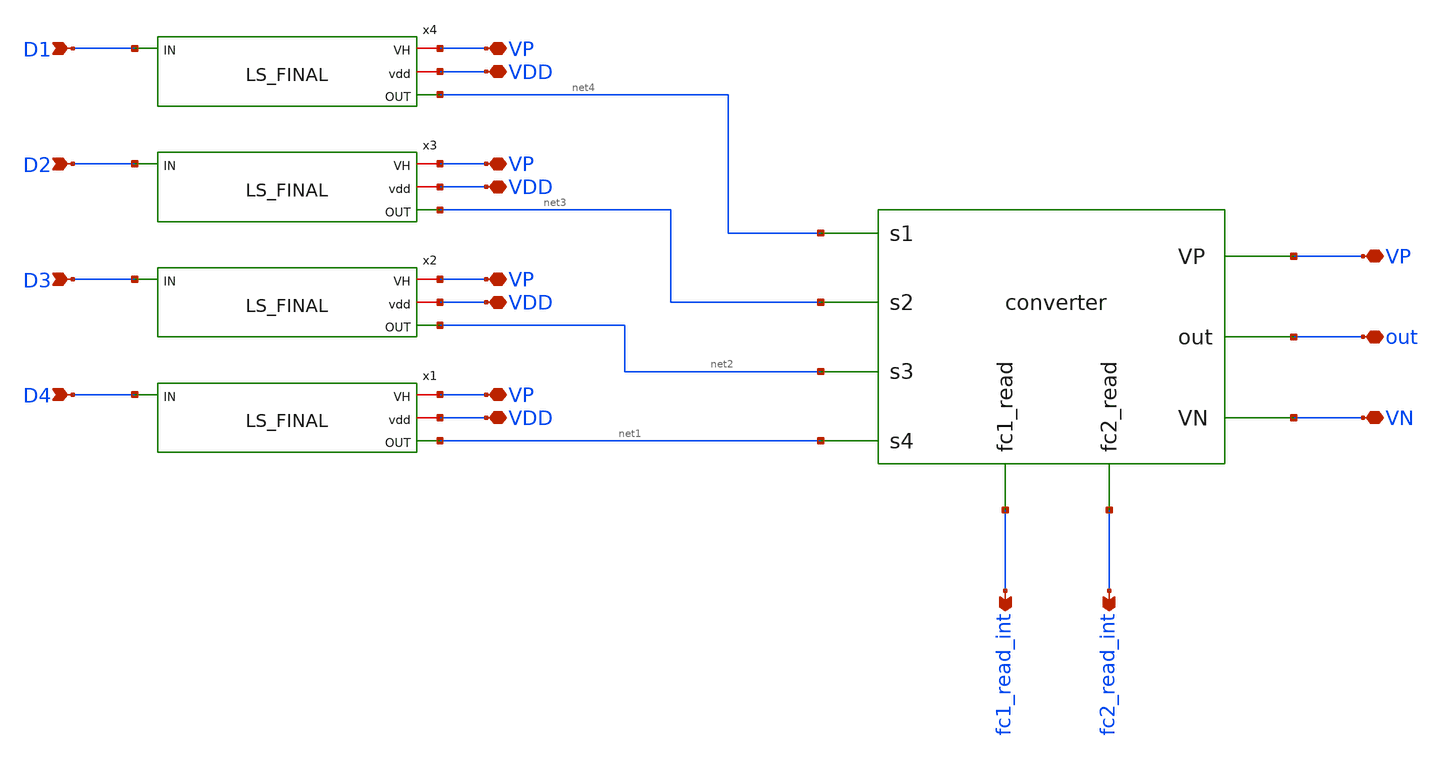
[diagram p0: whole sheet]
** sch_path: xschem/hierarchy_sch/interleaved.sch
**.subckt interleaved VN D1 D2 D3 D4 fc1_read_int fc2_read_int VP VP VP VP VP VDD VDD VDD VDD out
*.iopin VN
*.ipin D1
*.ipin D2
*.ipin D3
*.ipin D4
*.opin fc1_read_int
*.opin fc2_read_int
*.iopin VP
*.iopin VP
*.iopin VP
*.iopin VP
*.iopin VP
*.iopin VDD
*.iopin VDD
*.iopin VDD
*.iopin VDD
*.iopin out
x1 VP VDD net1 D4 LS_FINAL
x2 VP VDD net2 D3 LS_FINAL
x3 VP VDD net3 D2 LS_FINAL
x4 VP VDD net4 D1 LS_FINAL
X1 net4 net3 net2 net1 out VP VN fc1_read_int fc2_read_int converter
**.ends

* expanding   symbol:  personal/3LFCC_AC3E/xschem/dev_switches/DCDC_5V_FINAL/LS_FINAL.sym # of
*+ pins=4
** sym_path: xschem/dev_switches/DCDC_5V_FINAL/LS_FINAL.sym
** sch_path: xschem/dev_switches/DCDC_5V_FINAL/LS_FINAL.sch
.subckt LS_FINAL VH vdd OUT IN
*.ipin IN
*.iopin vdd
*.iopin VH
*.opin OUT
XM11 net1 IN vdd vdd sky130_fd_pr__pfet_01v8 L=0.15 W=5 nf=1 ad='int((nf+1)/2) * W/nf * 0.29' as='int((nf+2)/2) * W/nf * 0.29'
+ pd='2*int((nf+1)/2) * (W/nf + 0.29)' ps='2*int((nf+2)/2) * (W/nf + 0.29)' nrd='0.29 / W' nrs='0.29 / W'
+ sa=0 sb=0 sd=0 mult=1 m=1
XM12 net1 IN GND GND sky130_fd_pr__nfet_01v8 L=0.15 W=5 nf=1 ad='int((nf+1)/2) * W/nf * 0.29' as='int((nf+2)/2) * W/nf * 0.29'
+ pd='2*int((nf+1)/2) * (W/nf + 0.29)' ps='2*int((nf+2)/2) * (W/nf + 0.29)' nrd='0.29 / W' nrs='0.29 / W'
+ sa=0 sb=0 sd=0 mult=1 m=1
XM15 net2 net3 VH VH sky130_fd_pr__pfet_g5v0d10v5 L=0.5 W=2 nf=1 ad='int((nf+1)/2) * W/nf * 0.29' as='int((nf+2)/2) * W/nf * 0.29'
+ pd='2*int((nf+1)/2) * (W/nf + 0.29)' ps='2*int((nf+2)/2) * (W/nf + 0.29)' nrd='0.29 / W' nrs='0.29 / W'
+ sa=0 sb=0 sd=0 mult=1 m=1
XM14 net3 net2 VH VH sky130_fd_pr__pfet_g5v0d10v5 L=0.5 W=2 nf=1 ad='int((nf+1)/2) * W/nf * 0.29' as='int((nf+2)/2) * W/nf * 0.29'
+ pd='2*int((nf+1)/2) * (W/nf + 0.29)' ps='2*int((nf+2)/2) * (W/nf + 0.29)' nrd='0.29 / W' nrs='0.29 / W'
+ sa=0 sb=0 sd=0 mult=1 m=1
XM16 net4 net2 VH VH sky130_fd_pr__pfet_g5v0d10v5 L=0.5 W=10 nf=1 ad='int((nf+1)/2) * W/nf * 0.29' as='int((nf+2)/2) * W/nf * 0.29'
+ pd='2*int((nf+1)/2) * (W/nf + 0.29)' ps='2*int((nf+2)/2) * (W/nf + 0.29)' nrd='0.29 / W' nrs='0.29 / W'
+ sa=0 sb=0 sd=0 mult=10 m=10
XM18 net2 net1 GND GND sky130_fd_pr__nfet_g5v0d10v5 L=0.5 W=12 nf=1 ad='int((nf+1)/2) * W/nf * 0.29'
+ as='int((nf+2)/2) * W/nf * 0.29' pd='2*int((nf+1)/2) * (W/nf + 0.29)' ps='2*int((nf+2)/2) * (W/nf + 0.29)'
+ nrd='0.29 / W' nrs='0.29 / W' sa=0 sb=0 sd=0 mult=1 m=1
XM13 net3 IN GND GND sky130_fd_pr__nfet_g5v0d10v5 L=0.5 W=12 nf=1 ad='int((nf+1)/2) * W/nf * 0.29' as='int((nf+2)/2) * W/nf * 0.29'
+ pd='2*int((nf+1)/2) * (W/nf + 0.29)' ps='2*int((nf+2)/2) * (W/nf + 0.29)' nrd='0.29 / W' nrs='0.29 / W'
+ sa=0 sb=0 sd=0 mult=1 m=1
XM17 net4 IN GND GND sky130_fd_pr__nfet_g5v0d10v5 L=0.5 W=10 nf=1 ad='int((nf+1)/2) * W/nf * 0.29' as='int((nf+2)/2) * W/nf * 0.29'
+ pd='2*int((nf+1)/2) * (W/nf + 0.29)' ps='2*int((nf+2)/2) * (W/nf + 0.29)' nrd='0.29 / W' nrs='0.29 / W'
+ sa=0 sb=0 sd=0 mult=10 m=10
XM7 OUT net4 VH VH sky130_fd_pr__pfet_g5v0d10v5 L=0.5 W=10 nf=1 ad='int((nf+1)/2) * W/nf * 0.29' as='int((nf+2)/2) * W/nf * 0.29'
+ pd='2*int((nf+1)/2) * (W/nf + 0.29)' ps='2*int((nf+2)/2) * (W/nf + 0.29)' nrd='0.29 / W' nrs='0.29 / W'
+ sa=0 sb=0 sd=0 mult={multip} m={multip}
XM10 OUT net4 GND GND sky130_fd_pr__nfet_g5v0d10v5 L=0.5 W=10 nf=1 ad='int((nf+1)/2) * W/nf * 0.29' as='int((nf+2)/2) * W/nf * 0.29'
+ pd='2*int((nf+1)/2) * (W/nf + 0.29)' ps='2*int((nf+2)/2) * (W/nf + 0.29)' nrd='0.29 / W' nrs='0.29 / W'
+ sa=0 sb=0 sd=0 mult={multip} m={multip}
**** begin user architecture code

*
* Parameters

*.PARAM BAT=1.8
.PARAM W12=12 W45=2 LLS=0.5 multip=40
*.option scale=1e-6
*.options TEMP = 65.0

* Models
*.lib /foss/pdk/sky130A/libs.tech/ngspice/sky130.lib.spice TT

*Fuentes******
*VBAT VDD 0 DC BAT
*VHIGH VH 0 DC 5
*vin IN 0 dc 0 PULSE (0 BAT .1n .1n .1n 10n 20n)

*COUT OUT 0 20p


*.options savecurrents
*.save all
*+ @M.XM12.msky130_fd_pr_nfet_01v8[id]

*.control
*tran 0.1n 100n
*plot v(IN) v(LS1) v(OUT) v(net6) i(@M.XM12.msky130_fd_pr_nfet_01v8[id])
*write LS_FINAL.raw
*.endc
*.end
*

**** end user architecture code
.ends


* expanding   symbol:  personal/3LFCC_AC3E/xschem/hierarchy_sch/converter.sym # of pins=9
** sym_path: xschem/hierarchy_sch/converter.sym
** sch_path: xschem/hierarchy_sch/converter.sch
.subckt converter s1 s2 s3 s4 out VP VN fc1_read fc2_read
*.ipin s1
*.ipin s2
*.ipin s3
*.ipin s4
*.iopin VP
*.iopin VN
*.opin fc1_read
*.opin fc2_read
*.iopin out
X1v s1 s2 s3 s4 fc1_read net1 out VP VN power_stage
CFLY fc1_read fc2_read 6.8n m=1
R1 fc2_read net1 0.001 m=1
.ends


* expanding   symbol:  personal/3LFCC_AC3E/xschem/hierarchy_sch/power_stage.sym # of pins=9
** sym_path: xschem/hierarchy_sch/power_stage.sym
** sch_path: xschem/hierarchy_sch/power_stage.sch
.subckt power_stage s1 s2 s3 s4 fc1 fc2 out VP VN
*.ipin s1
*.ipin s2
*.ipin s3
*.ipin s4
*.iopin VP
*.iopin VN
*.opin out
*.opin fc1
*.opin fc2
X1 s2 fc1 s1 VP out transistor_group_one
X2 s4 fc2 s3 out VN transistor_group_two
.ends


* expanding   symbol:  personal/3LFCC_AC3E/xschem/hierarchy_sch/transistor_group_one.sym # of pins=5
** sym_path: xschem/hierarchy_sch/transistor_group_one.sym
** sch_path: xschem/hierarchy_sch/transistor_group_one.sch
.subckt transistor_group_one s2 fc1 s1 VP out
*.iopin VP
*.ipin s1
*.ipin s2
*.opin fc1
*.iopin out
XM3 out s2 fc1 fc1 sky130_fd_pr__pfet_g5v0d10v5 L=0.5 W=4.38 nf=1 ad='int((nf+1)/2) * W/nf * 0.29' as='int((nf+2)/2) * W/nf * 0.29'
+ pd='2*int((nf+1)/2) * (W/nf + 0.29)' ps='2*int((nf+2)/2) * (W/nf + 0.29)' nrd='0.29 / W' nrs='0.29 / W'
+ sa=0 sb=0 sd=0 mult=4506 m=4506
XM4 fc1 s1 VP VP sky130_fd_pr__pfet_g5v0d10v5 L=0.5 W=4.38 nf=1 ad='int((nf+1)/2) * W/nf * 0.29' as='int((nf+2)/2) * W/nf * 0.29'
+ pd='2*int((nf+1)/2) * (W/nf + 0.29)' ps='2*int((nf+2)/2) * (W/nf + 0.29)' nrd='0.29 / W' nrs='0.29 / W'
+ sa=0 sb=0 sd=0 mult=4506 m=4506
.ends


* expanding   symbol:  personal/3LFCC_AC3E/xschem/hierarchy_sch/transistor_group_two.sym # of pins=5
** sym_path: xschem/hierarchy_sch/transistor_group_two.sym
** sch_path: xschem/hierarchy_sch/transistor_group_two.sch
.subckt transistor_group_two s4 fc2 s3 out VN
*.iopin out
*.ipin s3
*.ipin s4
*.opin fc2
*.iopin VN
XM1 out s3 fc2 fc2 sky130_fd_pr__nfet_g5v0d10v5 L=0.5 W=4.38 nf=1 ad='int((nf+1)/2) * W/nf * 0.29' as='int((nf+2)/2) * W/nf * 0.29'
+ pd='2*int((nf+1)/2) * (W/nf + 0.29)' ps='2*int((nf+2)/2) * (W/nf + 0.29)' nrd='0.29 / W' nrs='0.29 / W'
+ sa=0 sb=0 sd=0 mult=2520 m=2520
XM2 fc2 s4 VN VN sky130_fd_pr__nfet_g5v0d10v5 L=0.5 W=4.38 nf=1 ad='int((nf+1)/2) * W/nf * 0.29' as='int((nf+2)/2) * W/nf * 0.29'
+ pd='2*int((nf+1)/2) * (W/nf + 0.29)' ps='2*int((nf+2)/2) * (W/nf + 0.29)' nrd='0.29 / W' nrs='0.29 / W'
+ sa=0 sb=0 sd=0 mult=2520 m=2520
.ends

.GLOBAL GND
.end
